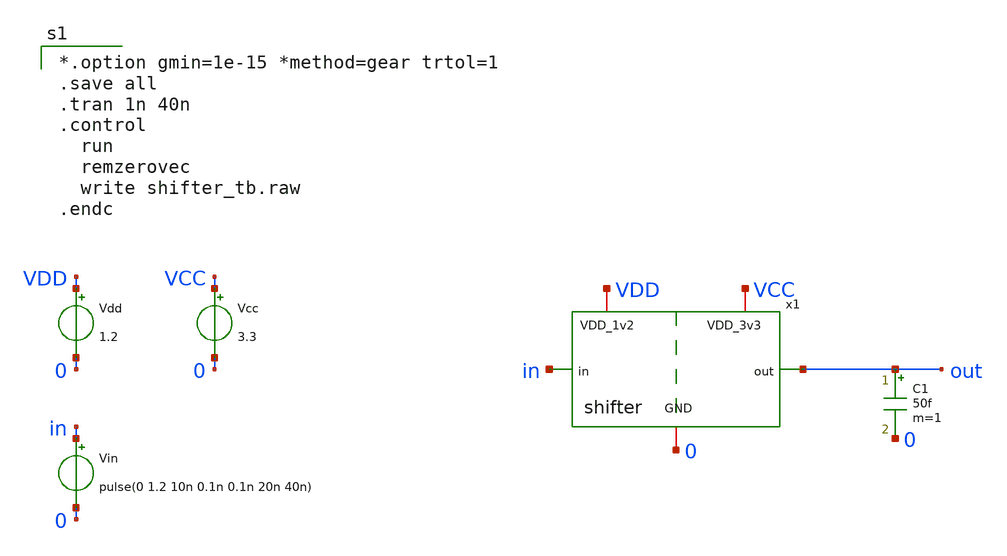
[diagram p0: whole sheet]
** sch_path: FLDO/design_data/xschem/shifter_tb.sch
**.subckt shifter_tb
Vdd VDD 0 1.2
Vcc VCC 0 3.3
Vin in 0 pulse(0 1.2 10n 0.1n 0.1n 20n 40n)
x1 VCC VDD 0 in out shifter
C1 out 0 50f m=1
**** begin user architecture code

*.option gmin=1e-15 *method=gear trtol=1
.save all
.tran 1n 40n
.control
  run
  remzerovec
  write shifter_tb.raw
.endc




** IHP models
.lib cornerMOSlv.lib mos_tt
.lib cornerMOShv.lib mos_tt
.lib cornerHBT.lib hbt_typ
.lib cornerRES.lib res_typ
.lib cornerCAP.lib cap_typ


**** end user architecture code
**.ends

* expanding   symbol:  shifter.sym # of pins=5
** sym_path: FLDO/design_data/xschem/shifter.sym
** sch_path: FLDO/design_data/xschem/shifter.sch
.subckt shifter VDD_3v3 VDD_1v2 GND in out
*.iopin VDD_3v3
*.iopin VDD_1v2
*.iopin GND
*.ipin in
*.opin out
XM1 lvlsh in_b GND GND sg13_hv_nmos w=2u l=0.45u ng=1 m=1 mm_ok=1
XM2 lvlsh_b in GND GND sg13_hv_nmos w=2u l=0.45u ng=1 m=1 mm_ok=1
XM3 lvlsh lvlsh_b VDD_3v3 VDD_3v3 sg13_hv_pmos w=0.3u l=0.45u ng=1 m=1 mm_ok=1
XM4 lvlsh_b lvlsh VDD_3v3 VDD_3v3 sg13_hv_pmos w=0.3u l=0.45u ng=1 m=1 mm_ok=1
XM5 in_b in GND GND sg13_lv_nmos w=0.74u l=0.13u ng=1 m=1 mm_ok=1
XM6 in_b in VDD_1v2 VDD_1v2 sg13_lv_pmos w=1.12u l=0.13u ng=1 m=1 mm_ok=1
XM7 out lvlsh_b GND GND sg13_hv_nmos w=2u l=0.45u ng=1 m=1 mm_ok=1
XM8 out lvlsh_b VDD_3v3 VDD_3v3 sg13_hv_pmos w=2u l=0.4u ng=1 m=2 mm_ok=1
.ends

.end
